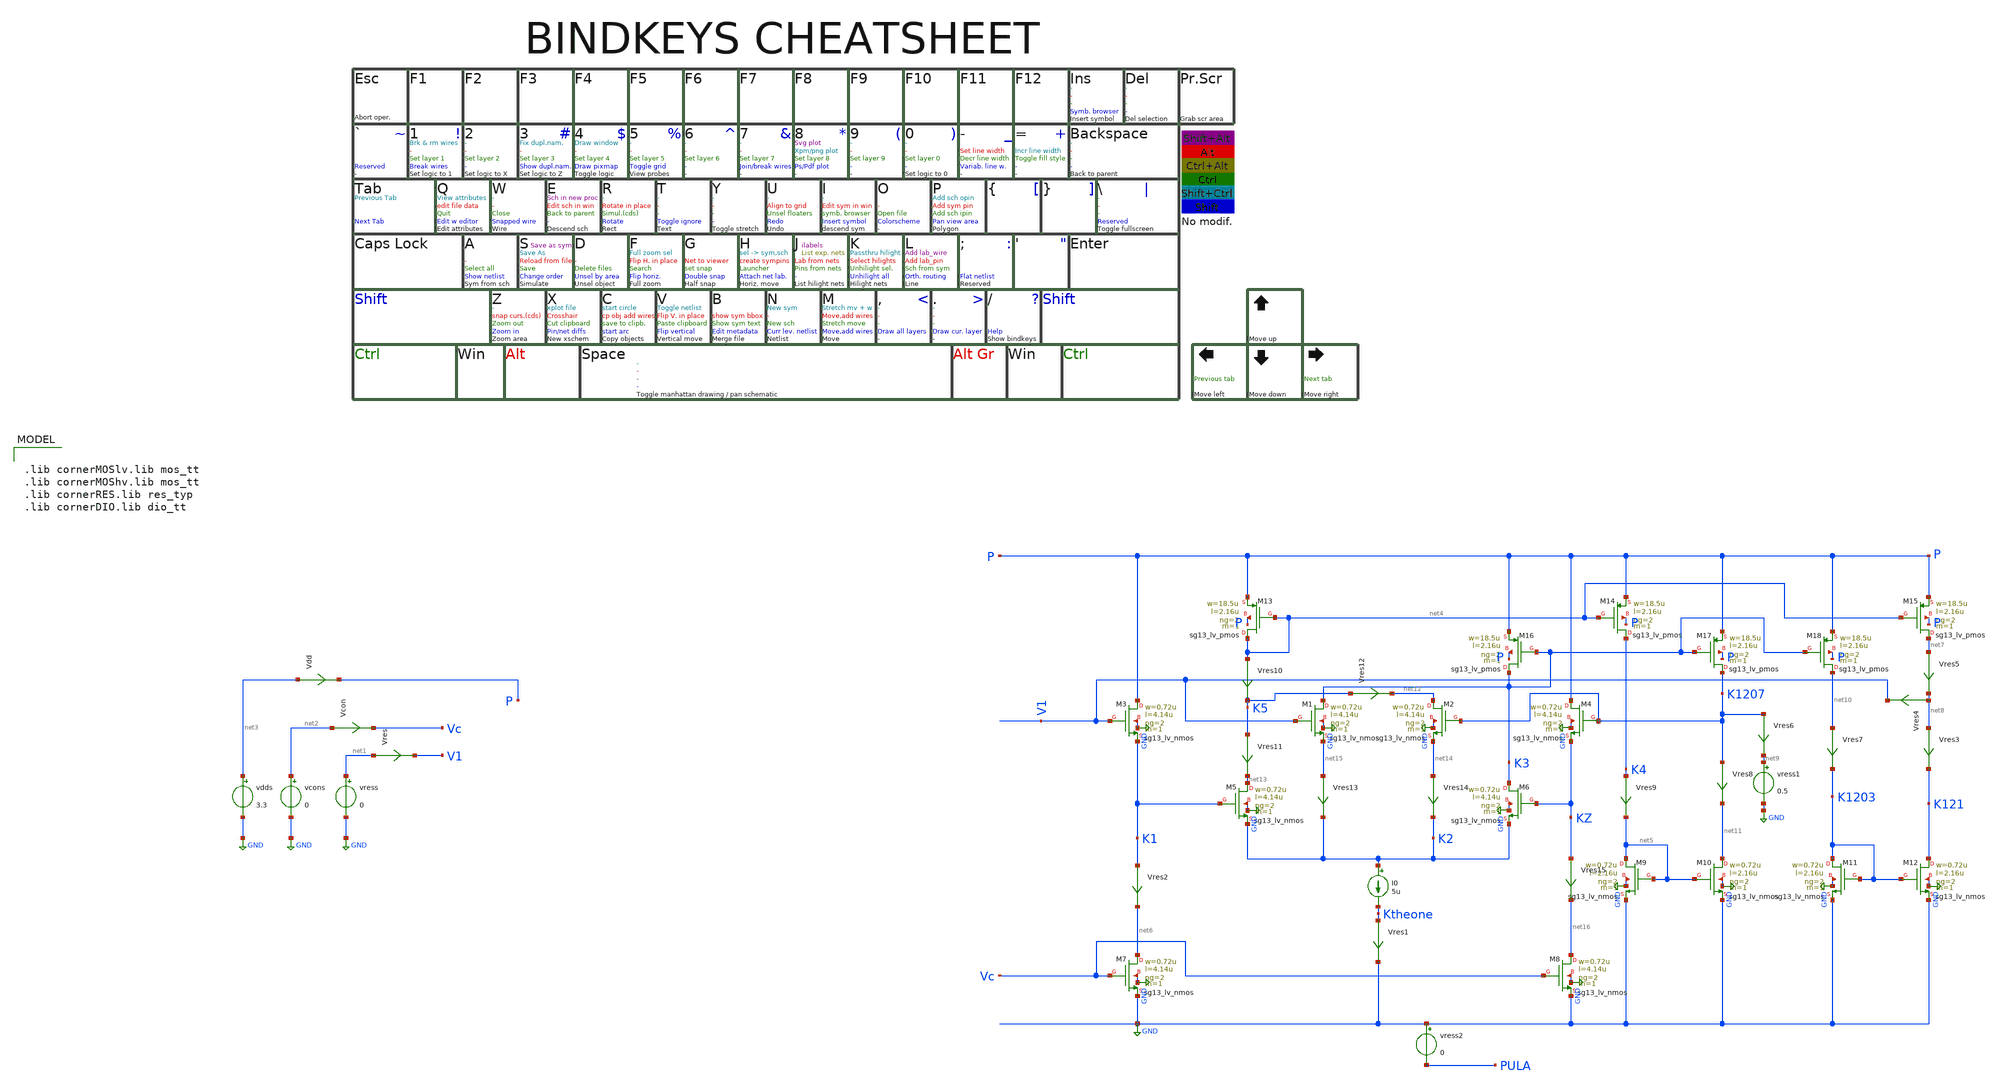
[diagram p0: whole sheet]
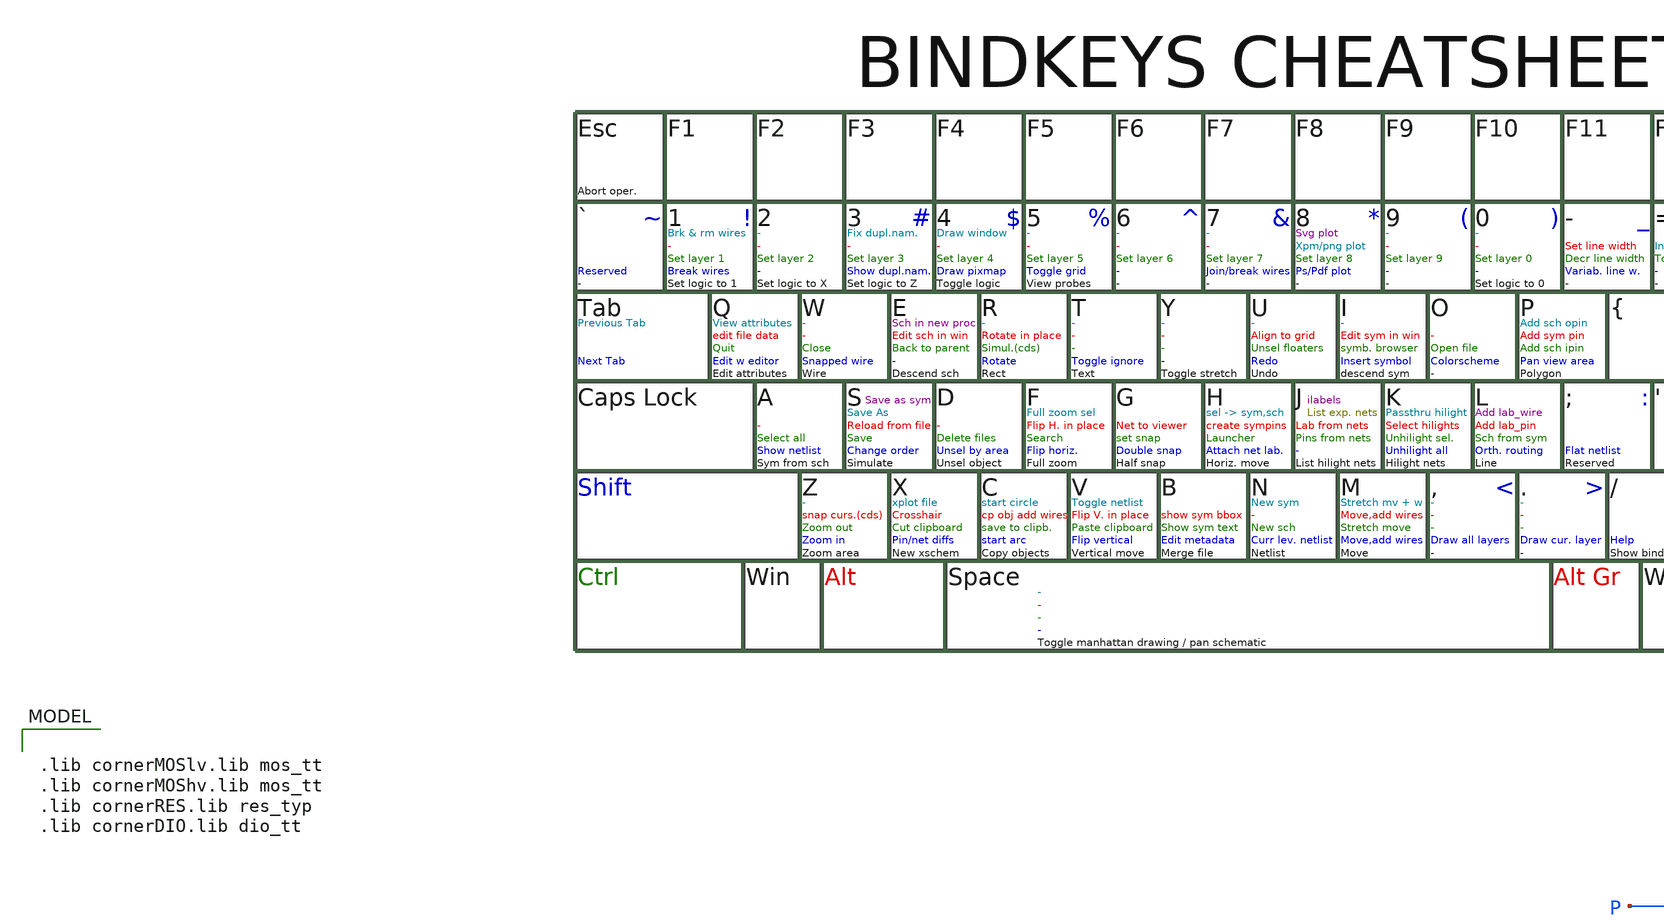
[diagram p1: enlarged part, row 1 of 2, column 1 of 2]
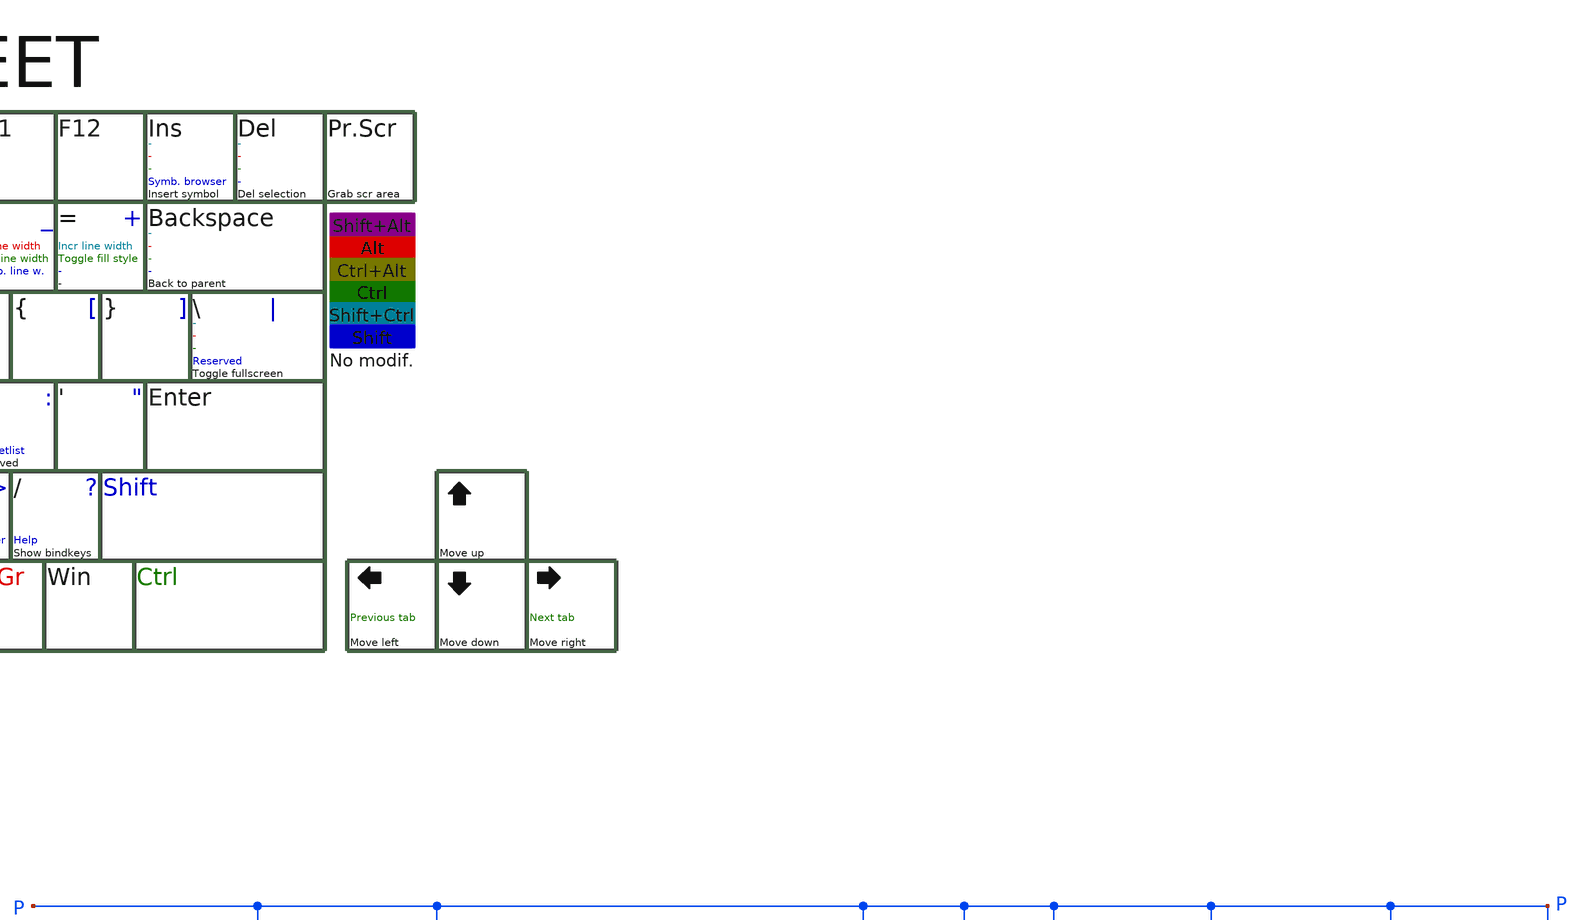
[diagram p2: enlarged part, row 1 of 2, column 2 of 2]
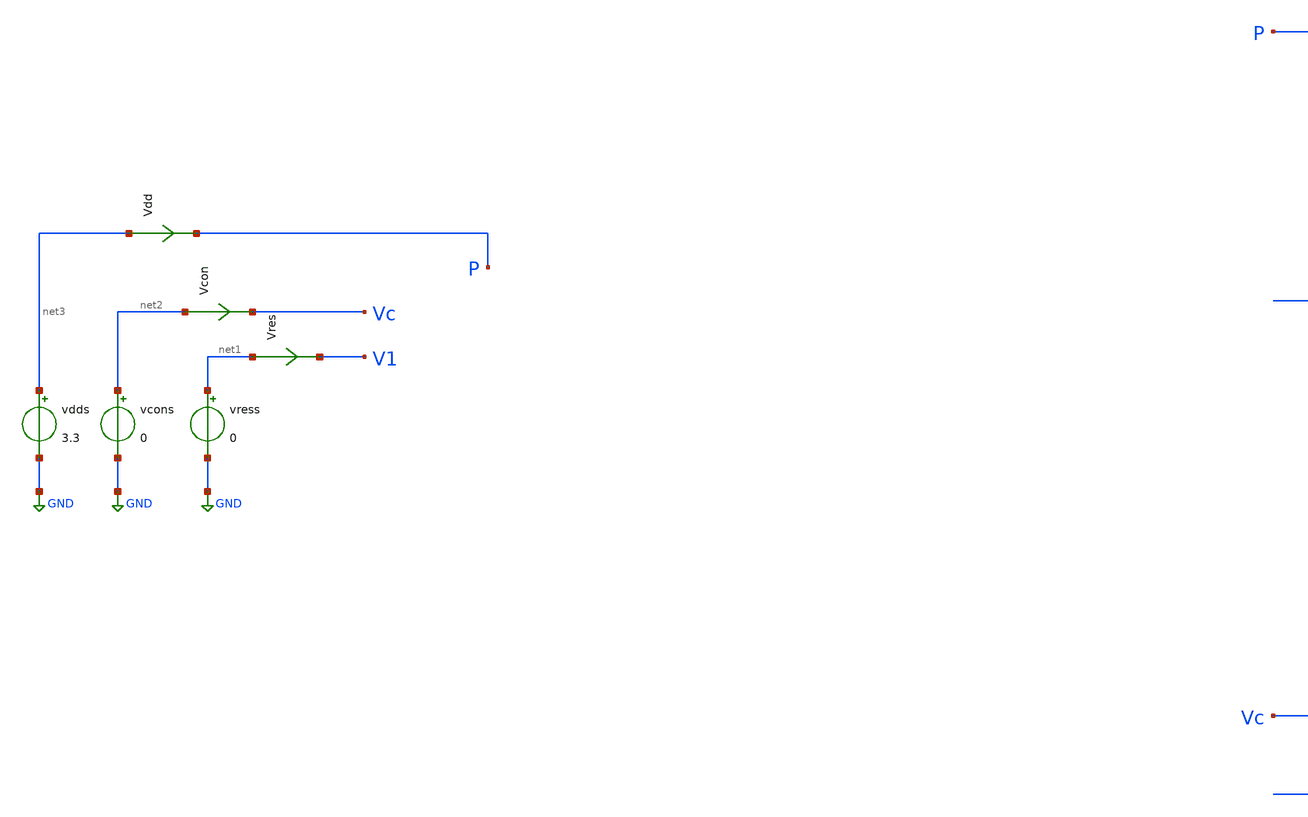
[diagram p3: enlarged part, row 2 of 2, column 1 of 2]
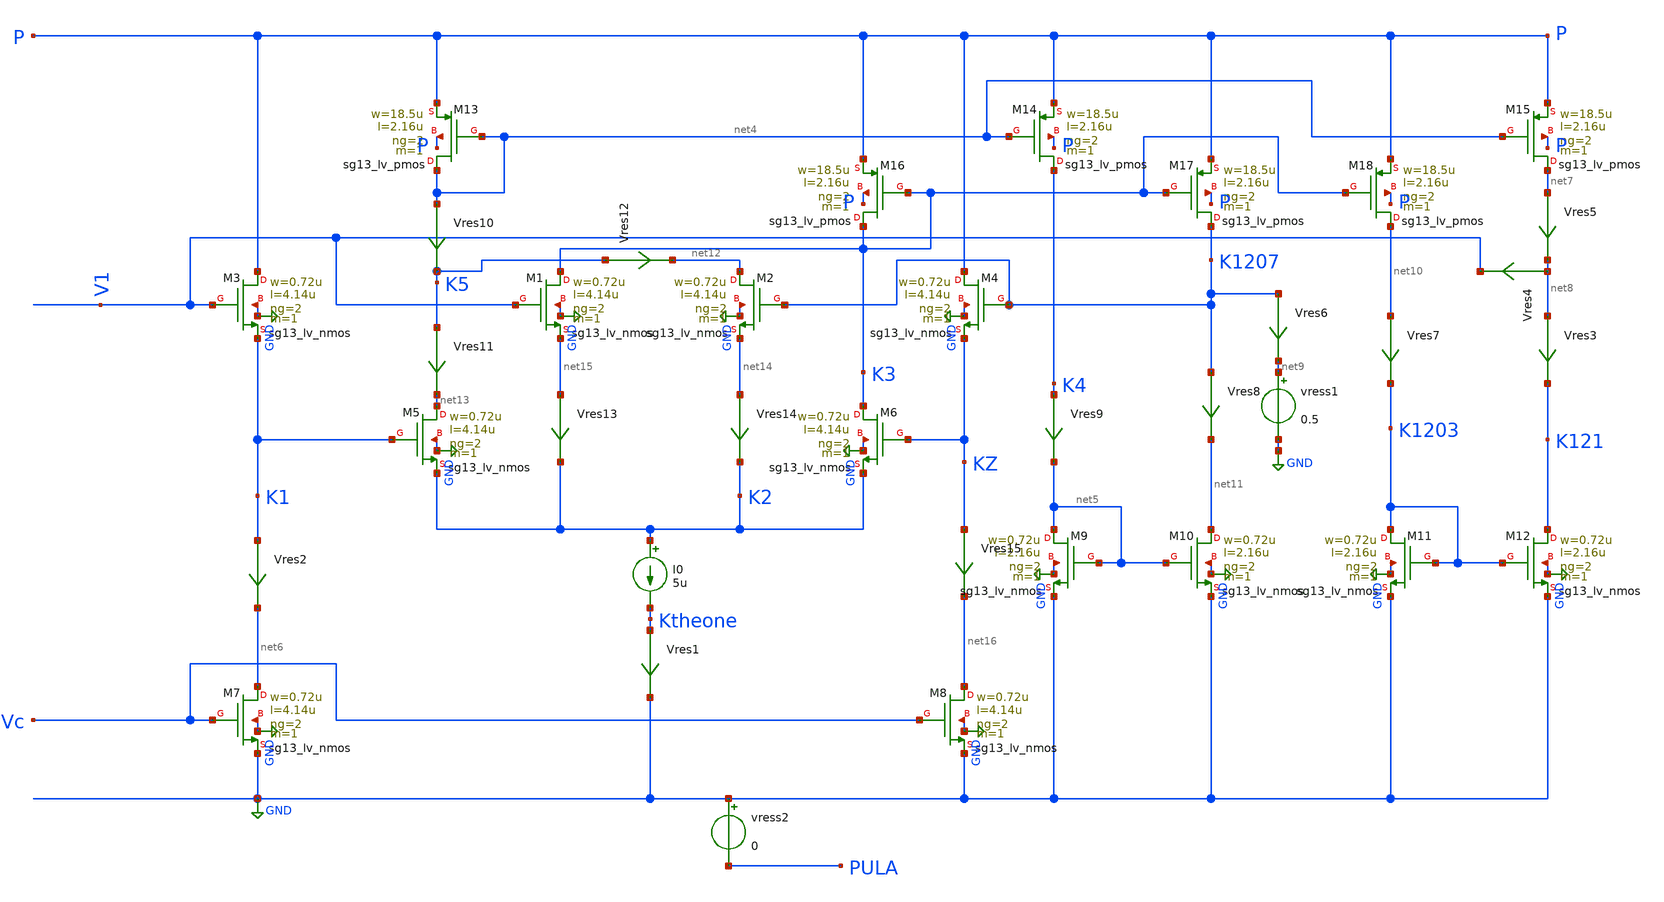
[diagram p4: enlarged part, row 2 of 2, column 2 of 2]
** sch_path: macros/heichips26_analog_project/macros/yadav/testbenches/xschem/plm.sch
**.subckt plm
Vres net1 V1 0
.save i(vres)
vress net1 GND 0
vcons net2 GND 0
vdds net3 GND 3.3
Vcon net2 Vc 0
.save i(vcon)
Vdd net3 P 0
.save i(vdd)
XM3 P V1 K1 GND sg13_lv_nmos w=0.72u l=4.14u ng=2 m=1 mm_ok=1
XM13 net4 net4 P P sg13_lv_pmos w=18.5u l=2.16u ng=2 m=1 mm_ok=1
XM1 K3 V1 net15 GND sg13_lv_nmos w=0.72u l=4.14u ng=2 m=1 mm_ok=1
XM5 net13 K1 K2 GND sg13_lv_nmos w=0.72u l=4.14u ng=2 m=1 mm_ok=1
XM2 net12 K1207 net14 GND sg13_lv_nmos w=0.72u l=4.14u ng=2 m=1 mm_ok=1
XM16 K3 K3 P P sg13_lv_pmos w=18.5u l=2.16u ng=2 m=1 mm_ok=1
XM7 net6 Vc GND GND sg13_lv_nmos w=0.72u l=4.14u ng=2 m=1 mm_ok=1
XM6 K3 KZ K2 GND sg13_lv_nmos w=0.72u l=4.14u ng=2 m=1 mm_ok=1
XM14 K4 net4 P P sg13_lv_pmos w=18.5u l=2.16u ng=2 m=1 mm_ok=1
XM8 net16 Vc GND GND sg13_lv_nmos w=0.72u l=4.14u ng=2 m=1 mm_ok=1
XM4 P K1207 KZ GND sg13_lv_nmos w=0.72u l=4.14u ng=2 m=1 mm_ok=1
XM9 net5 net5 GND GND sg13_lv_nmos w=0.72u l=2.16u ng=2 m=1 mm_ok=1
XM10 net11 net5 GND GND sg13_lv_nmos w=0.72u l=2.16u ng=2 m=1 mm_ok=1
XM17 K1207 K3 P P sg13_lv_pmos w=18.5u l=2.16u ng=2 m=1 mm_ok=1
XM18 net10 K3 P P sg13_lv_pmos w=18.5u l=2.16u ng=2 m=1 mm_ok=1
XM11 K1203 K1203 GND GND sg13_lv_nmos w=0.72u l=2.16u ng=2 m=1 mm_ok=1
XM12 K121 K1203 GND GND sg13_lv_nmos w=0.72u l=2.16u ng=2 m=1 mm_ok=1
XM15 net7 net4 P P sg13_lv_pmos w=18.5u l=2.16u ng=2 m=1 mm_ok=1
I0 K2 Ktheone 5u
Vres1 Ktheone GND 0
.save i(vres1)
Vres2 K1 net6 0
.save i(vres2)
Vres3 net8 K121 0
.save i(vres3)
Vres4 net8 V1 0
.save i(vres4)
Vres5 net7 net8 0
.save i(vres5)
vress1 net9 GND 0.5
Vres6 K1207 net9 0
.save i(vres6)
Vres7 net10 K1203 0
.save i(vres7)
Vres8 K1207 net11 0
.save i(vres8)
Vres9 K4 net5 0
.save i(vres9)
Vres10 net4 K5 0
.save i(vres10)
Vres11 K5 net13 0
.save i(vres11)
Vres12 K5 net12 0
.save i(vres12)
Vres13 net15 K2 0
.save i(vres13)
Vres14 net14 K2 0
.save i(vres14)
Vres15 KZ net16 0
.save i(vres15)
vress2 GND PULA 0
**** begin user architecture code


* .include ../../../netlist/pex/inverter_magic_pex_3.spice
.param temp=27
.options savecurrents klu method=gear reltol=1e-3 abstol=1e-15 gmin=1e-15
.control
save all
set appendwrite

* DC Sweep
* dc vcon 1 1.5 1m
* remzerovec

* plot v(vres)/i(Vres)
*plot v(VStage1)
*plot v(VStage2)



let vcc = 0
repeat 5
  alter vress $&vcc

  * DC Sweep
  dc vcons 0.3 1 1m
  remzerovec
  let vcc = vcc + 0.25
end
set appendwrite

* plot dc1.v(V1)/(dc1.i(Vres)) dc2.v(V1)/(dc2.i(Vres)) dc3.v(V1)/(dc3.i(Vres))
*+ dc4.v(V1)/(dc4.i(Vres)) dc5.v(V1)/(dc5.i(Vres))

plot (dc1.i(Vres)) (dc2.i(Vres)) (dc3.i(Vres)) (dc4.i(Vres)) (dc5.i(Vres))

plot (dc1.i(Vres6)) (dc2.i(Vres6)) (dc3.i(Vres6)) (dc4.i(Vres6)) (dc5.i(Vres6))


* Write Data
unset appendwrite
set wr_vecnames
set wr_singlescale

*quit
.endc



.lib cornerMOSlv.lib mos_tt
.lib cornerMOShv.lib mos_tt
.lib cornerRES.lib res_typ
.lib cornerDIO.lib dio_tt

**** end user architecture code
**.ends
.GLOBAL GND
.end
